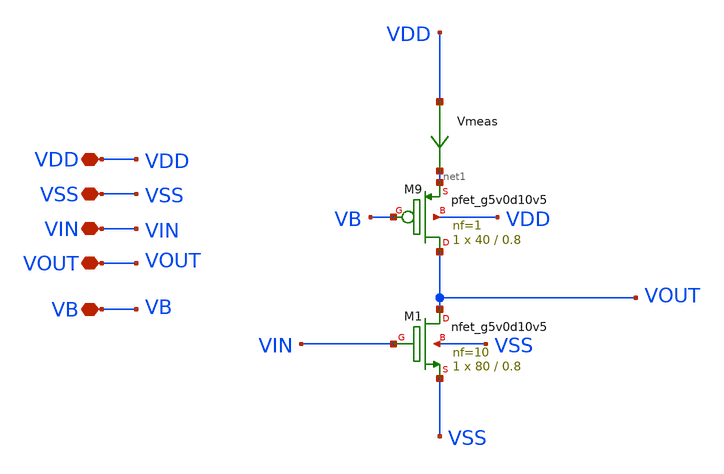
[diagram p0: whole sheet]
** sch_path: amplifiers/single_stage_amps/basic_stages/cs_current_pmos_stage/cs_current_pmos_stage.sch
**.subckt cs_current_pmos_stage VDD VSS VIN VOUT VB
*.iopin VDD
*.iopin VSS
*.iopin VIN
*.iopin VOUT
*.iopin VB
Vmeas VDD net1 0
.save i(vmeas)
XM1 VOUT VIN VSS VSS sky130_fd_pr__nfet_g5v0d10v5 L=0.8 W=80 nf=10 ad='int((10 + 1)/2) * 80 / 10 * 0.29'
+ as='int((10 + 2)/2) * 80 / 10 * 0.29' pd='2*int((10 + 1)/2) * (80 / 10 + 0.29)' ps='2*int((10 + 2)/2) * (80 / 10 + 0.29)'
+ nrd='0.29 / 80 ' nrs='0.29 / 80 ' sa=0 sb=0 sd=0 mult=1 m=1
XM9 VOUT VB net1 VDD sky130_fd_pr__pfet_g5v0d10v5 L=0.8 W=40 nf=1 ad='int((1 + 1)/2) * 40 / 1 * 0.29'
+ as='int((1 + 2)/2) * 40 / 1 * 0.29' pd='2*int((1 + 1)/2) * (40 / 1 + 0.29)' ps='2*int((1 + 2)/2) * (40 / 1 + 0.29)'
+ nrd='0.29 / 40 ' nrs='0.29 / 40 ' sa=0 sb=0 sd=0 mult=1 m=1
**.ends
.end
